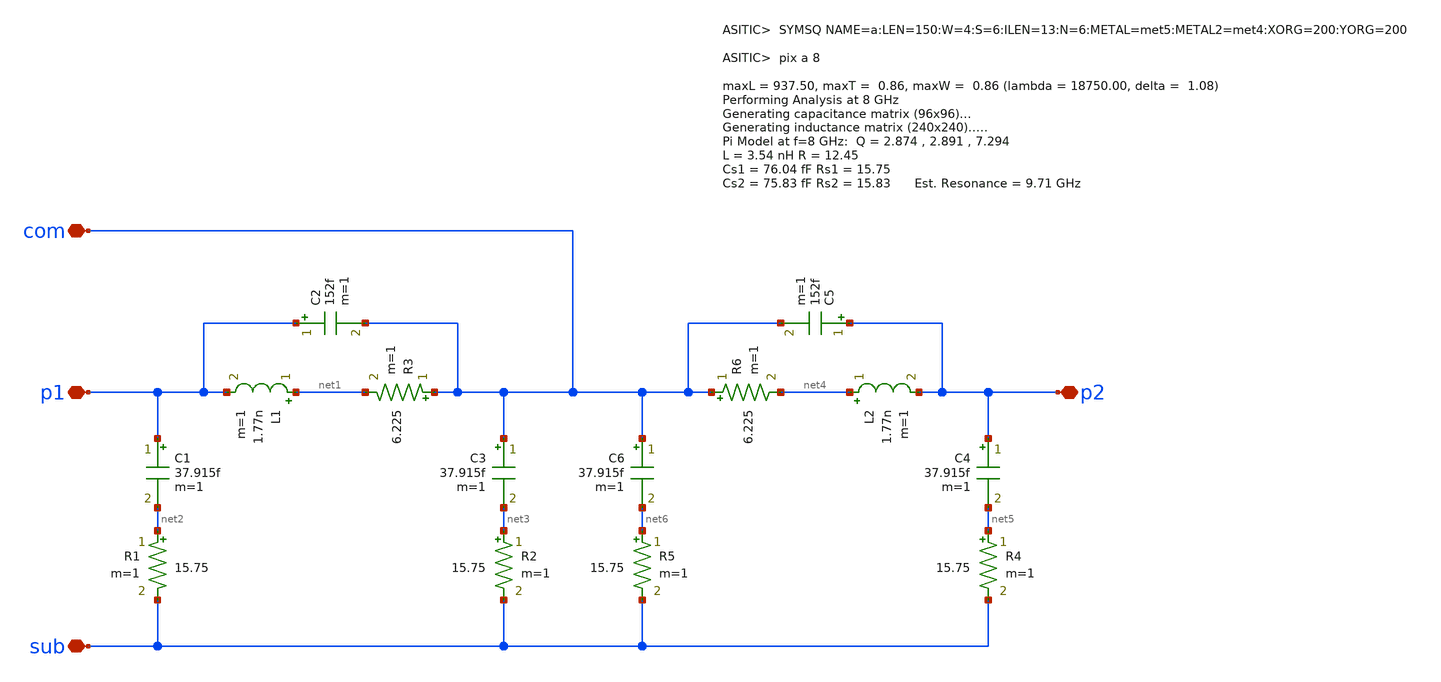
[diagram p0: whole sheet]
** sch_path: design/upconvert_inductor/upconvert_inductor.sch
**.subckt upconvert_inductor p2 p1 sub com
*.iopin p2
*.iopin p1
*.iopin sub
*.iopin com
L1 net1 p1 1.77n m=1
C1 p1 net2 37.915f m=1
R1 net2 sub 15.75 m=1
C2 p1 com 152f m=1
R3 com net1 6.225 m=1
L2 net4 p2 1.77n m=1
C4 p2 net5 37.915f m=1
R4 net5 sub 15.75 m=1
C5 p2 com 152f m=1
R6 com net4 6.225 m=1
C3 com net3 37.915f m=1
R2 net3 sub 15.75 m=1
C6 com net6 37.915f m=1
R5 net6 sub 15.75 m=1
**.ends
.end
